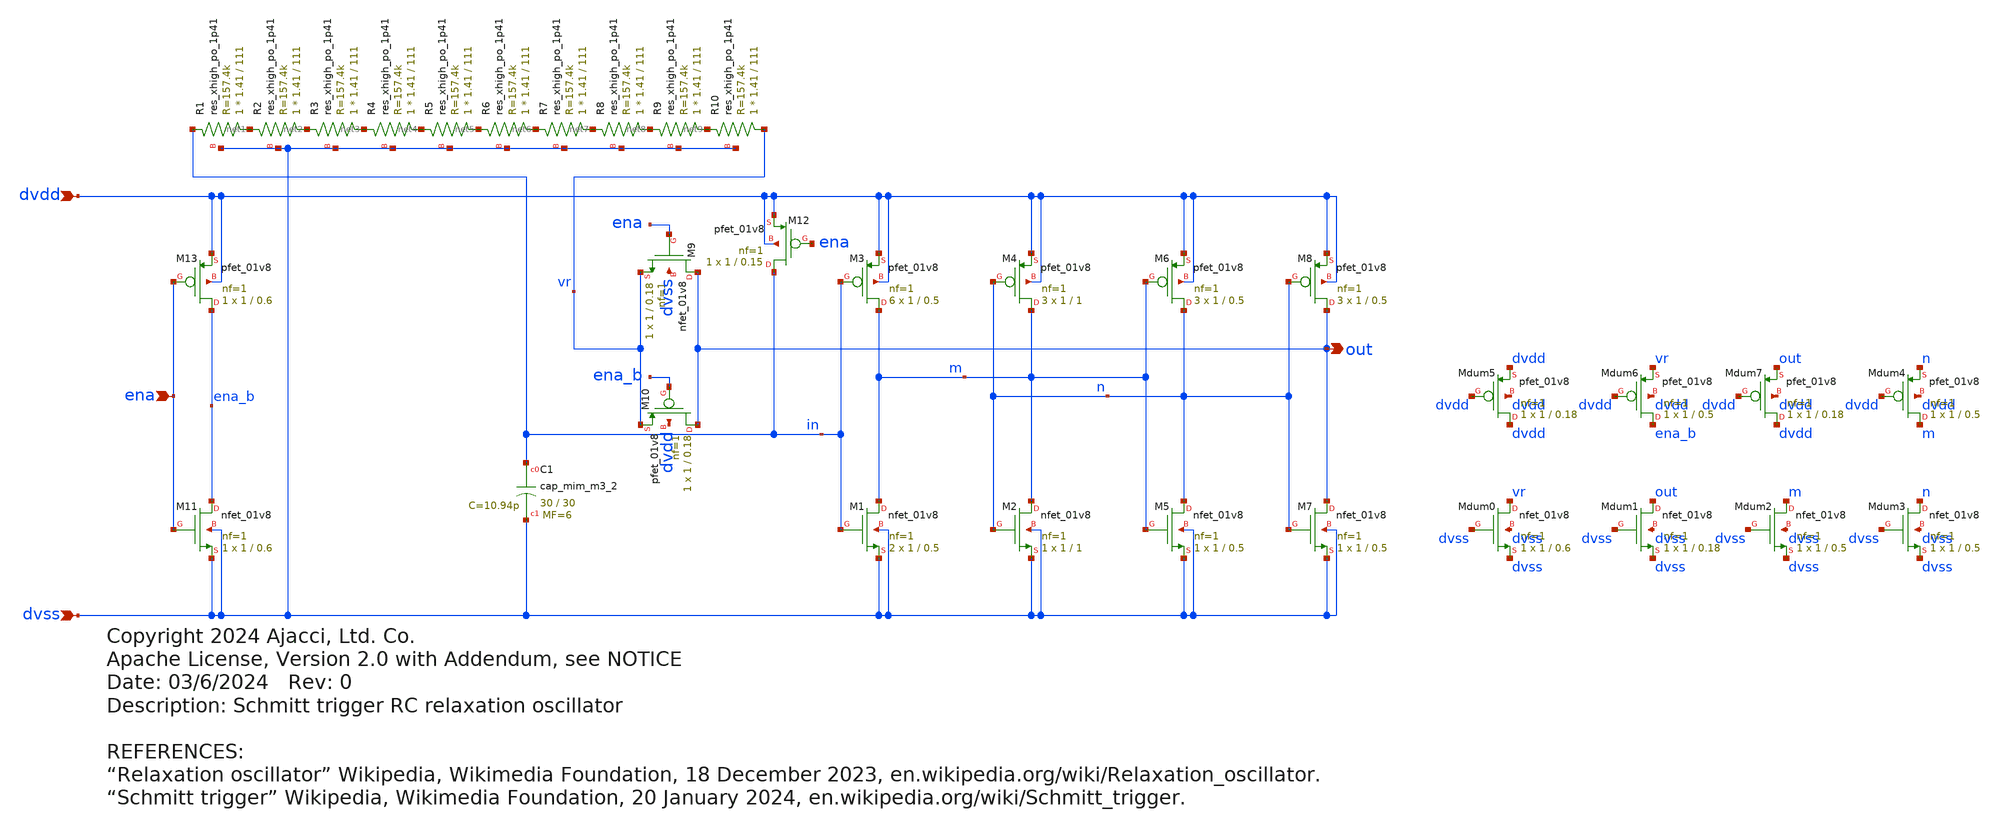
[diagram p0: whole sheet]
** sch_path: xschem/rc_osc.sch
* Copyright 2024 Ajacci, Ltd. Co.
* Apache License, Version 2.0 with Addendum, see NOTICE
**.subckt rc_osc dvdd dvss out ena
*.ipin dvdd
*.ipin dvss
*.opin out
*.ipin ena
XM1 m in dvss dvss sky130_fd_pr__nfet_01v8 L=0.5 W=1 nf=1 ad='int((nf+1)/2) * W/nf * 0.29' as='int((nf+2)/2) * W/nf * 0.29'
+ pd='2*int((nf+1)/2) * (W/nf + 0.29)' ps='2*int((nf+2)/2) * (W/nf + 0.29)' nrd='0.29 / W' nrs='0.29 / W'
+ sa=0 sb=0 sd=0 mult=2 m=2
XM3 m in dvdd dvdd sky130_fd_pr__pfet_01v8 L=0.5 W=1 nf=1 ad='int((nf+1)/2) * W/nf * 0.29' as='int((nf+2)/2) * W/nf * 0.29'
+ pd='2*int((nf+1)/2) * (W/nf + 0.29)' ps='2*int((nf+2)/2) * (W/nf + 0.29)' nrd='0.29 / W' nrs='0.29 / W'
+ sa=0 sb=0 sd=0 mult=6 m=6
XM2 m n dvss dvss sky130_fd_pr__nfet_01v8 L=1 W=1 nf=1 ad='int((nf+1)/2) * W/nf * 0.29' as='int((nf+2)/2) * W/nf * 0.29'
+ pd='2*int((nf+1)/2) * (W/nf + 0.29)' ps='2*int((nf+2)/2) * (W/nf + 0.29)' nrd='0.29 / W' nrs='0.29 / W'
+ sa=0 sb=0 sd=0 mult=1 m=1
XM4 m n dvdd dvdd sky130_fd_pr__pfet_01v8 L=1 W=1 nf=1 ad='int((nf+1)/2) * W/nf * 0.29' as='int((nf+2)/2) * W/nf * 0.29'
+ pd='2*int((nf+1)/2) * (W/nf + 0.29)' ps='2*int((nf+2)/2) * (W/nf + 0.29)' nrd='0.29 / W' nrs='0.29 / W'
+ sa=0 sb=0 sd=0 mult=3 m=3
XM5 n m dvss dvss sky130_fd_pr__nfet_01v8 L=0.5 W=1 nf=1 ad='int((nf+1)/2) * W/nf * 0.29' as='int((nf+2)/2) * W/nf * 0.29'
+ pd='2*int((nf+1)/2) * (W/nf + 0.29)' ps='2*int((nf+2)/2) * (W/nf + 0.29)' nrd='0.29 / W' nrs='0.29 / W'
+ sa=0 sb=0 sd=0 mult=1 m=1
XM6 n m dvdd dvdd sky130_fd_pr__pfet_01v8 L=0.5 W=1 nf=1 ad='int((nf+1)/2) * W/nf * 0.29' as='int((nf+2)/2) * W/nf * 0.29'
+ pd='2*int((nf+1)/2) * (W/nf + 0.29)' ps='2*int((nf+2)/2) * (W/nf + 0.29)' nrd='0.29 / W' nrs='0.29 / W'
+ sa=0 sb=0 sd=0 mult=3 m=3
XM7 out n dvss dvss sky130_fd_pr__nfet_01v8 L=0.5 W=1 nf=1 ad='int((nf+1)/2) * W/nf * 0.29' as='int((nf+2)/2) * W/nf * 0.29'
+ pd='2*int((nf+1)/2) * (W/nf + 0.29)' ps='2*int((nf+2)/2) * (W/nf + 0.29)' nrd='0.29 / W' nrs='0.29 / W'
+ sa=0 sb=0 sd=0 mult=1 m=1
XM8 out n dvdd dvdd sky130_fd_pr__pfet_01v8 L=0.5 W=1 nf=1 ad='int((nf+1)/2) * W/nf * 0.29' as='int((nf+2)/2) * W/nf * 0.29'
+ pd='2*int((nf+1)/2) * (W/nf + 0.29)' ps='2*int((nf+2)/2) * (W/nf + 0.29)' nrd='0.29 / W' nrs='0.29 / W'
+ sa=0 sb=0 sd=0 mult=3 m=3
XC1 in dvss sky130_fd_pr__cap_mim_m3_2 W=30 L=30 MF=6 m=6
XR1 net1 in dvss sky130_fd_pr__res_xhigh_po_1p41 L=111 mult=1 m=1
XM12 in ena dvdd dvdd sky130_fd_pr__pfet_01v8 L=0.15 W=1 nf=1 ad='int((nf+1)/2) * W/nf * 0.29' as='int((nf+2)/2) * W/nf * 0.29'
+ pd='2*int((nf+1)/2) * (W/nf + 0.29)' ps='2*int((nf+2)/2) * (W/nf + 0.29)' nrd='0.29 / W' nrs='0.29 / W'
+ sa=0 sb=0 sd=0 mult=1 m=1
XM9 out ena vr dvss sky130_fd_pr__nfet_01v8 L=0.18 W=1 nf=1 ad='int((nf+1)/2) * W/nf * 0.29' as='int((nf+2)/2) * W/nf * 0.29'
+ pd='2*int((nf+1)/2) * (W/nf + 0.29)' ps='2*int((nf+2)/2) * (W/nf + 0.29)' nrd='0.29 / W' nrs='0.29 / W'
+ sa=0 sb=0 sd=0 mult=1 m=1
XM10 out ena_b vr dvdd sky130_fd_pr__pfet_01v8 L=0.18 W=1 nf=1 ad='int((nf+1)/2) * W/nf * 0.29' as='int((nf+2)/2) * W/nf * 0.29'
+ pd='2*int((nf+1)/2) * (W/nf + 0.29)' ps='2*int((nf+2)/2) * (W/nf + 0.29)' nrd='0.29 / W' nrs='0.29 / W'
+ sa=0 sb=0 sd=0 mult=1 m=1
XM11 ena_b ena dvss dvss sky130_fd_pr__nfet_01v8 L=0.6 W=1 nf=1 ad='int((nf+1)/2) * W/nf * 0.29' as='int((nf+2)/2) * W/nf * 0.29'
+ pd='2*int((nf+1)/2) * (W/nf + 0.29)' ps='2*int((nf+2)/2) * (W/nf + 0.29)' nrd='0.29 / W' nrs='0.29 / W'
+ sa=0 sb=0 sd=0 mult=1 m=1
XM13 ena_b ena dvdd dvdd sky130_fd_pr__pfet_01v8 L=0.6 W=1 nf=1 ad='int((nf+1)/2) * W/nf * 0.29' as='int((nf+2)/2) * W/nf * 0.29'
+ pd='2*int((nf+1)/2) * (W/nf + 0.29)' ps='2*int((nf+2)/2) * (W/nf + 0.29)' nrd='0.29 / W' nrs='0.29 / W'
+ sa=0 sb=0 sd=0 mult=1 m=1
XR2 net2 net1 dvss sky130_fd_pr__res_xhigh_po_1p41 L=111 mult=1 m=1
XR3 net3 net2 dvss sky130_fd_pr__res_xhigh_po_1p41 L=111 mult=1 m=1
XR4 net4 net3 dvss sky130_fd_pr__res_xhigh_po_1p41 L=111 mult=1 m=1
XR5 net5 net4 dvss sky130_fd_pr__res_xhigh_po_1p41 L=111 mult=1 m=1
XR6 net6 net5 dvss sky130_fd_pr__res_xhigh_po_1p41 L=111 mult=1 m=1
XR7 net7 net6 dvss sky130_fd_pr__res_xhigh_po_1p41 L=111 mult=1 m=1
XR8 net8 net7 dvss sky130_fd_pr__res_xhigh_po_1p41 L=111 mult=1 m=1
XR9 net9 net8 dvss sky130_fd_pr__res_xhigh_po_1p41 L=111 mult=1 m=1
XR10 vr net9 dvss sky130_fd_pr__res_xhigh_po_1p41 L=111 mult=1 m=1
XMdum0 vr dvss dvss dvss sky130_fd_pr__nfet_01v8 L=0.6 W=1 nf=1 ad='int((nf+1)/2) * W/nf * 0.29' as='int((nf+2)/2) * W/nf * 0.29'
+ pd='2*int((nf+1)/2) * (W/nf + 0.29)' ps='2*int((nf+2)/2) * (W/nf + 0.29)' nrd='0.29 / W' nrs='0.29 / W'
+ sa=0 sb=0 sd=0 mult=1 m=1
XMdum1 out dvss dvss dvss sky130_fd_pr__nfet_01v8 L=0.18 W=1 nf=1 ad='int((nf+1)/2) * W/nf * 0.29' as='int((nf+2)/2) * W/nf * 0.29'
+ pd='2*int((nf+1)/2) * (W/nf + 0.29)' ps='2*int((nf+2)/2) * (W/nf + 0.29)' nrd='0.29 / W' nrs='0.29 / W'
+ sa=0 sb=0 sd=0 mult=1 m=1
XMdum2 m dvss dvss dvss sky130_fd_pr__nfet_01v8 L=0.5 W=1 nf=1 ad='int((nf+1)/2) * W/nf * 0.29' as='int((nf+2)/2) * W/nf * 0.29'
+ pd='2*int((nf+1)/2) * (W/nf + 0.29)' ps='2*int((nf+2)/2) * (W/nf + 0.29)' nrd='0.29 / W' nrs='0.29 / W'
+ sa=0 sb=0 sd=0 mult=1 m=1
XMdum3 n dvss dvss dvss sky130_fd_pr__nfet_01v8 L=0.5 W=1 nf=1 ad='int((nf+1)/2) * W/nf * 0.29' as='int((nf+2)/2) * W/nf * 0.29'
+ pd='2*int((nf+1)/2) * (W/nf + 0.29)' ps='2*int((nf+2)/2) * (W/nf + 0.29)' nrd='0.29 / W' nrs='0.29 / W'
+ sa=0 sb=0 sd=0 mult=1 m=1
XMdum4 m dvdd n dvdd sky130_fd_pr__pfet_01v8 L=0.5 W=1 nf=1 ad='int((nf+1)/2) * W/nf * 0.29' as='int((nf+2)/2) * W/nf * 0.29'
+ pd='2*int((nf+1)/2) * (W/nf + 0.29)' ps='2*int((nf+2)/2) * (W/nf + 0.29)' nrd='0.29 / W' nrs='0.29 / W'
+ sa=0 sb=0 sd=0 mult=1 m=1
XMdum5 dvdd dvdd dvdd dvdd sky130_fd_pr__pfet_01v8 L=0.18 W=1 nf=1 ad='int((nf+1)/2) * W/nf * 0.29' as='int((nf+2)/2) * W/nf * 0.29'
+ pd='2*int((nf+1)/2) * (W/nf + 0.29)' ps='2*int((nf+2)/2) * (W/nf + 0.29)' nrd='0.29 / W' nrs='0.29 / W'
+ sa=0 sb=0 sd=0 mult=1 m=1
XMdum6 ena_b dvdd vr dvdd sky130_fd_pr__pfet_01v8 L=0.5 W=1 nf=1 ad='int((nf+1)/2) * W/nf * 0.29' as='int((nf+2)/2) * W/nf * 0.29'
+ pd='2*int((nf+1)/2) * (W/nf + 0.29)' ps='2*int((nf+2)/2) * (W/nf + 0.29)' nrd='0.29 / W' nrs='0.29 / W'
+ sa=0 sb=0 sd=0 mult=1 m=1
XMdum7 dvdd dvdd out dvdd sky130_fd_pr__pfet_01v8 L=0.18 W=1 nf=1 ad='int((nf+1)/2) * W/nf * 0.29' as='int((nf+2)/2) * W/nf * 0.29'
+ pd='2*int((nf+1)/2) * (W/nf + 0.29)' ps='2*int((nf+2)/2) * (W/nf + 0.29)' nrd='0.29 / W' nrs='0.29 / W'
+ sa=0 sb=0 sd=0 mult=1 m=1
**.ends
.end
